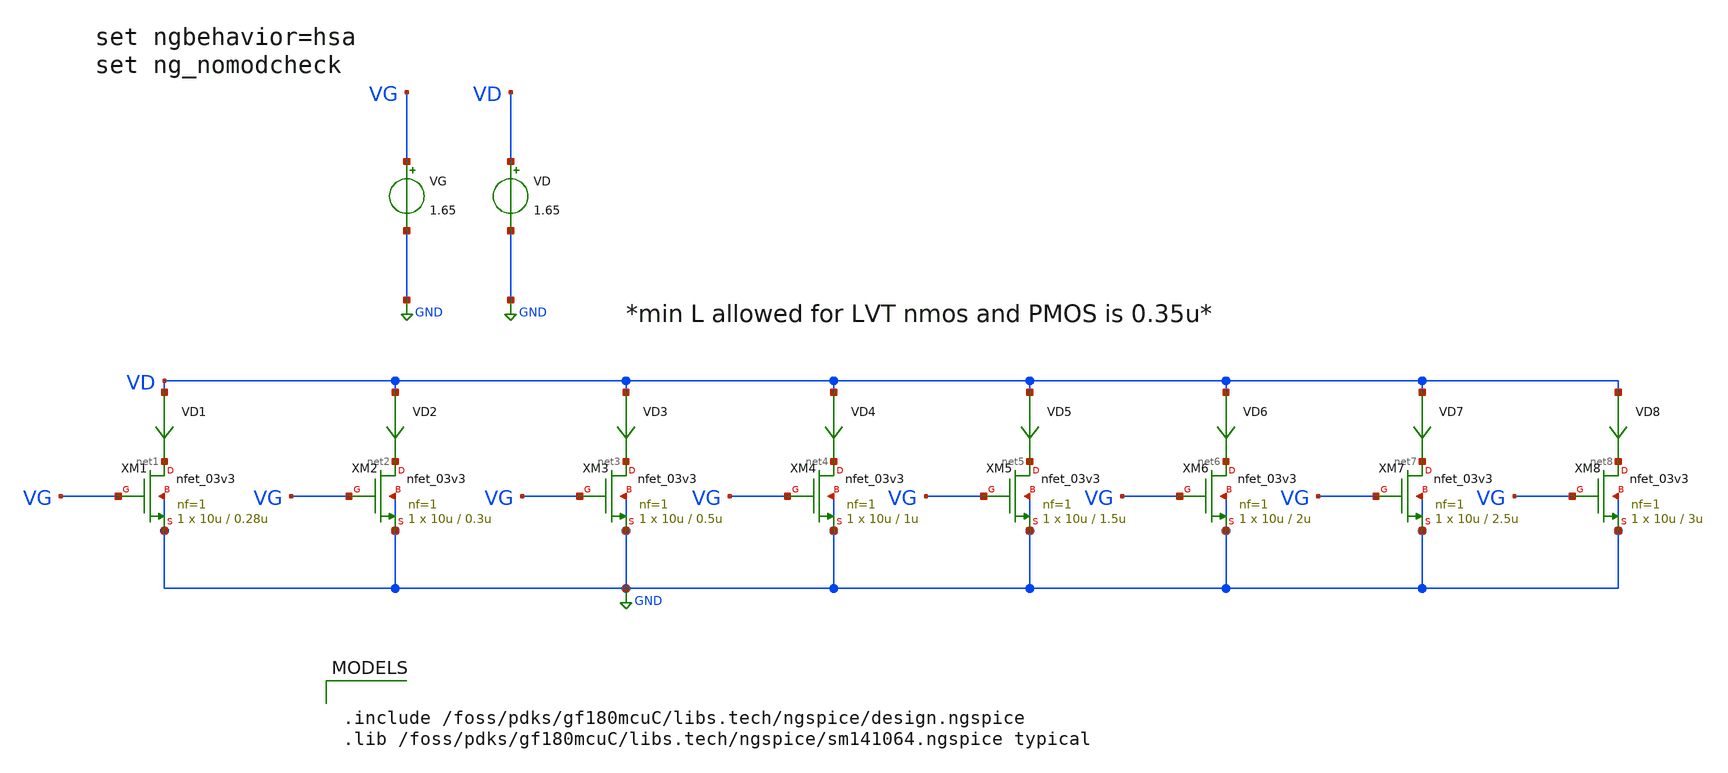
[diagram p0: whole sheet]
** sch_path: Testbench/gmid_nmos_01v8_lvt_tb.sch
**.subckt gmid_nmos_01v8_lvt_tb
VG VG GND 1.65
VD VD GND 1.65
VD1 VD net1 0
.save i(vd1)
VD2 VD net2 0
.save i(vd2)
VD3 VD net3 0
.save i(vd3)
VD4 VD net4 0
.save i(vd4)
VD5 VD net5 0
.save i(vd5)
XM2 net2 VG GND GND nfet_03v3 L=0.3u W=10u nf=1 ad='int((nf+1)/2) * W/nf * 0.18u' as='int((nf+2)/2) * W/nf * 0.18u'
+ pd='2*int((nf+1)/2) * (W/nf + 0.18u)' ps='2*int((nf+2)/2) * (W/nf + 0.18u)' nrd='0.18u / W' nrs='0.18u / W'
+ sa=0 sb=0 sd=0 m=1
XM1 net1 VG GND GND nfet_03v3 L=0.28u W=10u nf=1 ad='int((nf+1)/2) * W/nf * 0.18u' as='int((nf+2)/2) * W/nf * 0.18u'
+ pd='2*int((nf+1)/2) * (W/nf + 0.18u)' ps='2*int((nf+2)/2) * (W/nf + 0.18u)' nrd='0.18u / W' nrs='0.18u / W'
+ sa=0 sb=0 sd=0 m=1
XM3 net3 VG GND GND nfet_03v3 L=0.5u W=10u nf=1 ad='int((nf+1)/2) * W/nf * 0.18u' as='int((nf+2)/2) * W/nf * 0.18u'
+ pd='2*int((nf+1)/2) * (W/nf + 0.18u)' ps='2*int((nf+2)/2) * (W/nf + 0.18u)' nrd='0.18u / W' nrs='0.18u / W'
+ sa=0 sb=0 sd=0 m=1
XM4 net4 VG GND GND nfet_03v3 L=1u W=10u nf=1 ad='int((nf+1)/2) * W/nf * 0.18u' as='int((nf+2)/2) * W/nf * 0.18u'
+ pd='2*int((nf+1)/2) * (W/nf + 0.18u)' ps='2*int((nf+2)/2) * (W/nf + 0.18u)' nrd='0.18u / W' nrs='0.18u / W'
+ sa=0 sb=0 sd=0 m=1
XM5 net5 VG GND GND nfet_03v3 L=1.5u W=10u nf=1 ad='int((nf+1)/2) * W/nf * 0.18u' as='int((nf+2)/2) * W/nf * 0.18u'
+ pd='2*int((nf+1)/2) * (W/nf + 0.18u)' ps='2*int((nf+2)/2) * (W/nf + 0.18u)' nrd='0.18u / W' nrs='0.18u / W'
+ sa=0 sb=0 sd=0 m=1
VD6 VD net6 0
.save i(vd6)
XM6 net6 VG GND GND nfet_03v3 L=2u W=10u nf=1 ad='int((nf+1)/2) * W/nf * 0.18u' as='int((nf+2)/2) * W/nf * 0.18u'
+ pd='2*int((nf+1)/2) * (W/nf + 0.18u)' ps='2*int((nf+2)/2) * (W/nf + 0.18u)' nrd='0.18u / W' nrs='0.18u / W'
+ sa=0 sb=0 sd=0 m=1
VD7 VD net7 0
.save i(vd7)
XM7 net7 VG GND GND nfet_03v3 L=2.5u W=10u nf=1 ad='int((nf+1)/2) * W/nf * 0.18u' as='int((nf+2)/2) * W/nf * 0.18u'
+ pd='2*int((nf+1)/2) * (W/nf + 0.18u)' ps='2*int((nf+2)/2) * (W/nf + 0.18u)' nrd='0.18u / W' nrs='0.18u / W'
+ sa=0 sb=0 sd=0 m=1
VD8 VD net8 0
.save i(vd8)
XM8 net8 VG GND GND nfet_03v3 L=3u W=10u nf=1 ad='int((nf+1)/2) * W/nf * 0.18u' as='int((nf+2)/2) * W/nf * 0.18u'
+ pd='2*int((nf+1)/2) * (W/nf + 0.18u)' ps='2*int((nf+2)/2) * (W/nf + 0.18u)' nrd='0.18u / W' nrs='0.18u / W'
+ sa=0 sb=0 sd=0 m=1
**** begin user architecture code


* ngspice commands
.option wnflag=1
.option savecurrents
.control
save all
save @m.xm1.m0[gm]
save @m.xm2.m0[gm]
save @m.xm3.m0[gm]
save @m.xm4.m0[gm]
save @m.xm5.m0[gm]
save @m.xm6.m0[gm]
save @m.xm7.m0[gm]
save @m.xm8.m0[gm]
save @m.xm1.m0[vth]
save @m.xm2.m0[vth]
save @m.xm3.m0[vth]
save @m.xm4.m0[vth]
save @m.xm5.m0[vth]
save @m.xm6.m0[vth]
save @m.xm7.m0[vth]
save @m.xm8.m0[vth]
save @m.xm1.m0[gds]
save @m.xm2.m0[gds]
save @m.xm3.m0[gds]
save @m.xm4.m0[gds]
save @m.xm5.m0[gds]
save @m.xm6.m0[gds]
save @m.xm7.m0[gds]
save @m.xm8.m0[gds]
save @m.xm1.m0[cgg]
save @m.xm2.m0[cgg]
save @m.xm3.m0[cgg]
save @m.xm4.m0[cgg]
save @m.xm5.m0[cgg]
save @m.xm6.m0[cgg]
save @m.xm7.m0[cgg]
save @m.xm8.m0[cgg]
save @m.xm1.m0[cgd]
save @m.xm2.m0[cgd]
save @m.xm3.m0[cgd]
save @m.xm4.m0[cgd]
save @m.xm5.m0[cgd]
save @m.xm6.m0[cgd]
save @m.xm7.m0[cgd]
save @m.xm8.m0[cgd]
save @m.xm1.m0[cgs]
save @m.xm2.m0[cgs]
save @m.xm3.m0[cgs]
save @m.xm4.m0[cgs]
save @m.xm5.m0[cgs]
save @m.xm6.m0[cgs]
save @m.xm7.m0[cgs]
save @m.xm8.m0[cgs]

dc VG 0.05 3.3 0.05
** remove zero length vectors to prevent write errors
remzerovec
write /foss/designs/gf180mcu-sim/gmid_nmos_tb.raw
plot @m.xm1.m0[gm]
plot @m.xm2.m0[gm]
plot @m.xm3.m0[gm]
plot @m.xm4.m0[gm]
plot @m.xm5.m0[gm]
plot @m.xm6.m0[gm]
plot @m.xm7.m0[gm]
plot @m.xm8.m0[gm]

wrdata /foss/designs/gf180mcu-sim/gmid_nmos_1_nfet_01v8_lvt_tb.txt @m.xm1.m0[gm] i(VD1)
+ @m.xm1.m0[vth] @m.xm1.m0[gds] @m.xm1.m0[cgg] @m.xm1.m0[cgs] @m.xm1.m0[cgd]
wrdata /foss/designs/gf180mcu-sim/gmid_nmos_2_nfet_01v8_lvt_tb.txt @m.xm2.m0[gm] i(VD2)
+ @m.xm2.m0[vth] @m.xm2.m0[gds] @m.xm2.m0[cgg] @m.xm2.m0[cgs] @m.xm2.m0[cgd]
wrdata /foss/designs/gf180mcu-sim/gmid_nmos_3_nfet_01v8_lvt_tb.txt @m.xm3.m0[gm] i(VD3)
+ @m.xm3.m0[vth] @m.xm3.m0[gds] @m.xm3.m0[cgg] @m.xm3.m0[cgs] @m.xm3.m0[cgd]
wrdata /foss/designs/gf180mcu-sim/gmid_nmos_4_nfet_01v8_lvt_tb.txt @m.xm4.m0[gm] i(VD4)
+ @m.xm4.m0[vth] @m.xm4.m0[gds] @m.xm4.m0[cgg] @m.xm4.m0[cgs] @m.xm4.m0[cgd]
wrdata /foss/designs/gf180mcu-sim/gmid_nmos_5_nfet_01v8_lvt_tb.txt @m.xm5.m0[gm] i(VD5)
+ @m.xm5.m0[vth] @m.xm5.m0[gds] @m.xm5.m0[cgg] @m.xm5.m0[cgs] @m.xm5.m0[cgd]
wrdata /foss/designs/gf180mcu-sim/gmid_nmos_6_nfet_01v8_lvt_tb.txt @m.xm6.m0[gm] i(VD6)
+ @m.xm6.m0[vth] @m.xm6.m0[gds] @m.xm6.m0[cgg] @m.xm6.m0[cgs] @m.xm6.m0[cgd]
wrdata /foss/designs/gf180mcu-sim/gmid_nmos_7_nfet_01v8_lvt_tb.txt @m.xm7.m0[gm] i(VD7)
+ @m.xm7.m0[vth] @m.xm7.m0[gds] @m.xm7.m0[cgg] @m.xm7.m0[cgs] @m.xm7.m0[cgd]
wrdata /foss/designs/gf180mcu-sim/gmid_nmos_8_nfet_01v8_lvt_tb.txt @m.xm8.m0[gm] i(VD8)
+ @m.xm8.m0[vth] @m.xm8.m0[gds] @m.xm8.m0[cgg] @m.xm8.m0[cgs] @m.xm8.m0[cgd]

remzerovec
write /foss/designs/gf180mcu-sim/gmid_nmos_tb.raw
quit 0
.endc



.include /foss/pdks/gf180mcuC/libs.tech/ngspice/design.ngspice
.lib /foss/pdks/gf180mcuC/libs.tech/ngspice/sm141064.ngspice typical

**** end user architecture code
**.ends
.GLOBAL GND
.end
